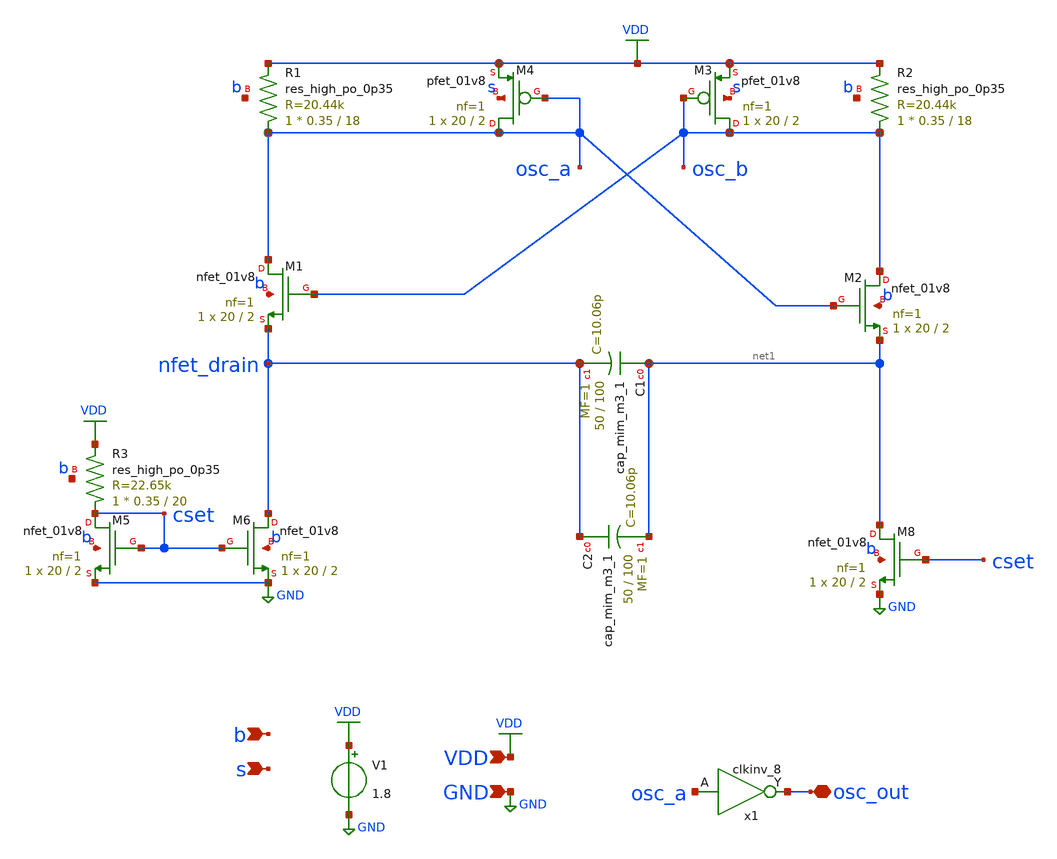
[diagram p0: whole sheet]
** sch_path: xschem/osc.sch
**.subckt osc VDD osc_out GND b s
*.ipin VDD
*.iopin osc_out
*.ipin GND
*.ipin b
*.ipin s
XM1 osc_a osc_b nfet_drain b sky130_fd_pr__nfet_01v8 L=2 W=20 nf=1 ad='int((nf+1)/2) * W/nf * 0.29' as='int((nf+2)/2) * W/nf * 0.29'
+ pd='2*int((nf+1)/2) * (W/nf + 0.29)' ps='2*int((nf+2)/2) * (W/nf + 0.29)' nrd='0.29 / W' nrs='0.29 / W'
+ sa=0 sb=0 sd=0 mult=1 m=1
XM2 osc_b osc_a net1 b sky130_fd_pr__nfet_01v8 L=2 W=20 nf=1 ad='int((nf+1)/2) * W/nf * 0.29' as='int((nf+2)/2) * W/nf * 0.29'
+ pd='2*int((nf+1)/2) * (W/nf + 0.29)' ps='2*int((nf+2)/2) * (W/nf + 0.29)' nrd='0.29 / W' nrs='0.29 / W'
+ sa=0 sb=0 sd=0 mult=1 m=1
XM3 osc_b osc_b VDD s sky130_fd_pr__pfet_01v8 L=2 W=20 nf=1 ad='int((nf+1)/2) * W/nf * 0.29' as='int((nf+2)/2) * W/nf * 0.29'
+ pd='2*int((nf+1)/2) * (W/nf + 0.29)' ps='2*int((nf+2)/2) * (W/nf + 0.29)' nrd='0.29 / W' nrs='0.29 / W'
+ sa=0 sb=0 sd=0 mult=1 m=1
XM4 osc_a osc_a VDD s sky130_fd_pr__pfet_01v8 L=2 W=20 nf=1 ad='int((nf+1)/2) * W/nf * 0.29' as='int((nf+2)/2) * W/nf * 0.29'
+ pd='2*int((nf+1)/2) * (W/nf + 0.29)' ps='2*int((nf+2)/2) * (W/nf + 0.29)' nrd='0.29 / W' nrs='0.29 / W'
+ sa=0 sb=0 sd=0 mult=1 m=1
XR1 osc_a VDD b sky130_fd_pr__res_high_po_0p35 L=18 mult=1 m=1
XR2 osc_b VDD b sky130_fd_pr__res_high_po_0p35 L=18 mult=1 m=1
XC1 net1 nfet_drain sky130_fd_pr__cap_mim_m3_1 W=50 L=100 MF=1 m=1
XM5 cset cset GND b sky130_fd_pr__nfet_01v8 L=2 W=20 nf=1 ad='int((nf+1)/2) * W/nf * 0.29' as='int((nf+2)/2) * W/nf * 0.29'
+ pd='2*int((nf+1)/2) * (W/nf + 0.29)' ps='2*int((nf+2)/2) * (W/nf + 0.29)' nrd='0.29 / W' nrs='0.29 / W'
+ sa=0 sb=0 sd=0 mult=1 m=1
XM6 nfet_drain cset GND b sky130_fd_pr__nfet_01v8 L=2 W=20 nf=1 ad='int((nf+1)/2) * W/nf * 0.29' as='int((nf+2)/2) * W/nf * 0.29'
+ pd='2*int((nf+1)/2) * (W/nf + 0.29)' ps='2*int((nf+2)/2) * (W/nf + 0.29)' nrd='0.29 / W' nrs='0.29 / W'
+ sa=0 sb=0 sd=0 mult=1 m=1
XR3 cset VDD b sky130_fd_pr__res_high_po_0p35 L=20 mult=1 m=1
XM8 net1 cset GND b sky130_fd_pr__nfet_01v8 L=2 W=20 nf=1 ad='int((nf+1)/2) * W/nf * 0.29' as='int((nf+2)/2) * W/nf * 0.29'
+ pd='2*int((nf+1)/2) * (W/nf + 0.29)' ps='2*int((nf+2)/2) * (W/nf + 0.29)' nrd='0.29 / W' nrs='0.29 / W'
+ sa=0 sb=0 sd=0 mult=1 m=1
x1 osc_a GND VGND VDD VDD osc_out sky130_fd_sc_hd__clkinv_8
XC2 nfet_drain net1 sky130_fd_pr__cap_mim_m3_1 W=50 L=100 MF=1 m=1
V1 VDD GND 1.8
**** begin user architecture code

** opencircuitdesign pdks install
.lib $::SKYWATER_MODELS/sky130.lib.spice tt
.include $::SKYWATER_STDCELLS/sky130_fd_sc_hd.spice





vs s 1.8 0
vb b 0 0

.control
tran 500p 5u uic
write testbench.raw
quit 0
.endc
.end


**** end user architecture code
**.ends
.GLOBAL GND
.GLOBAL VDD
.end
